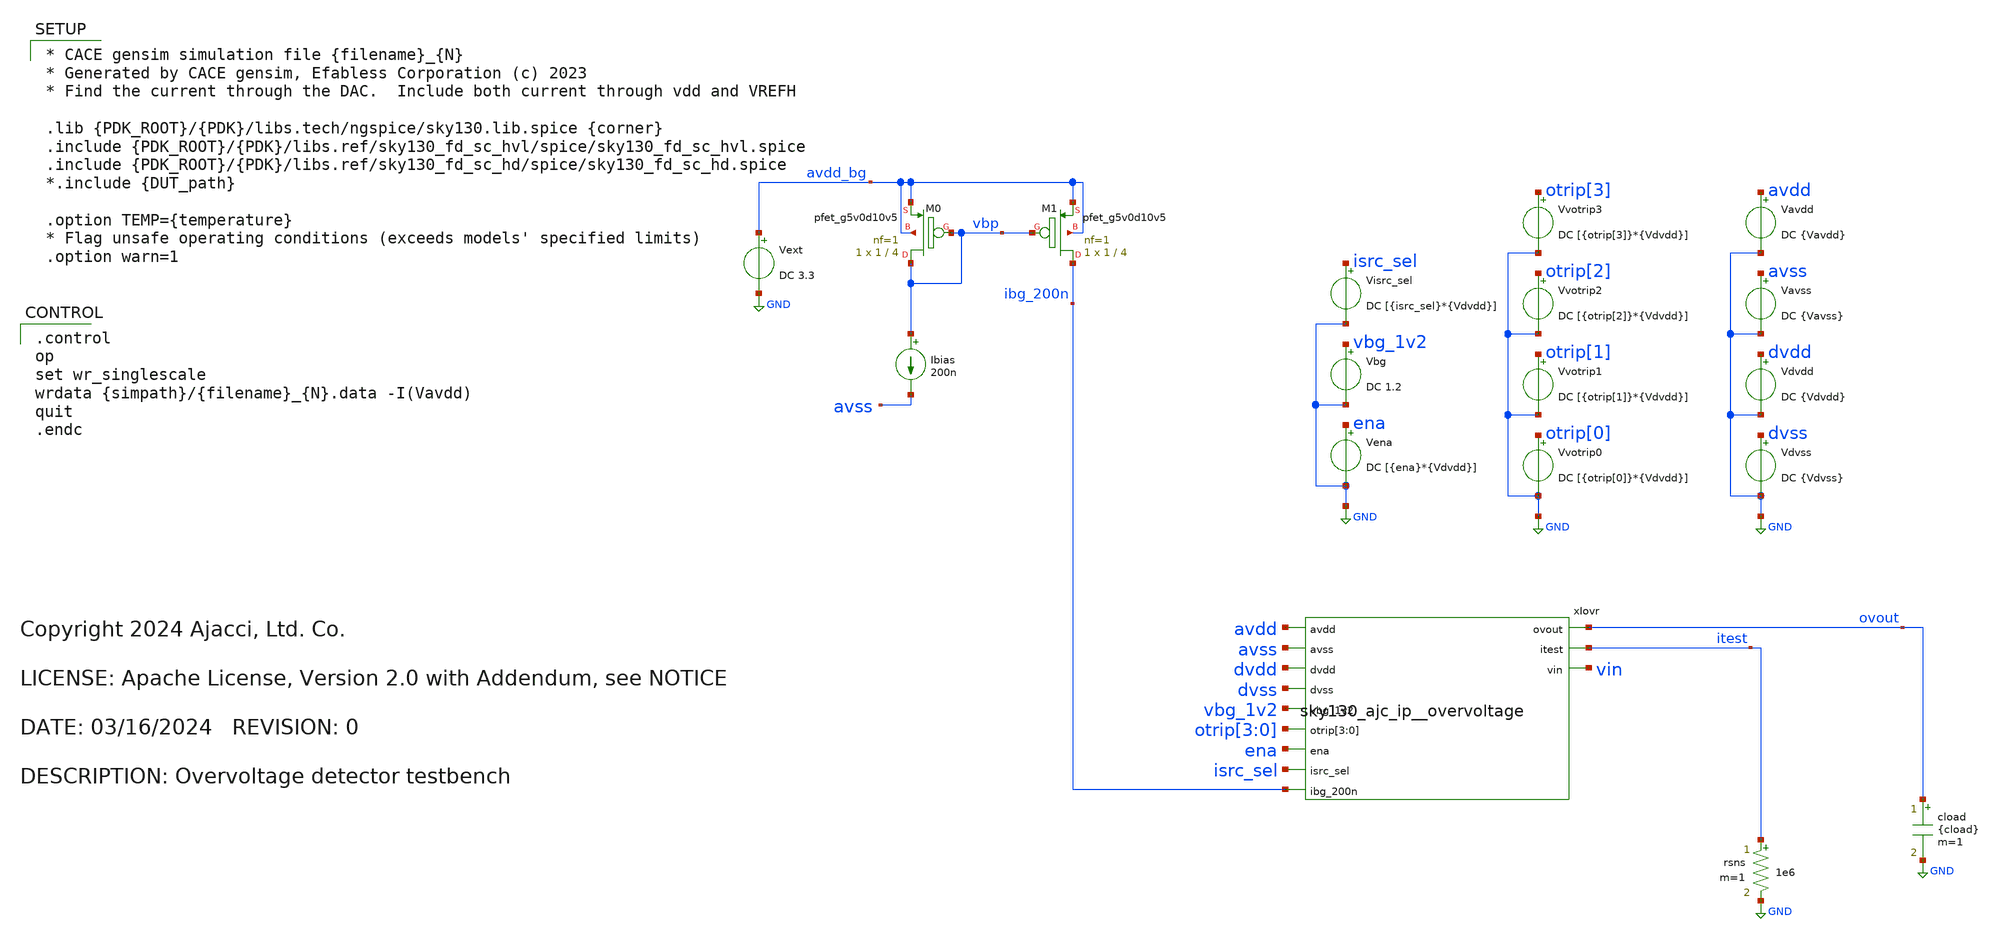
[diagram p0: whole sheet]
** sch_path: cace/dccurrent_avdd.sch
* Copyright 2024 Ajacci, Ltd. Co.
* LICENSE: Apache License, Version 2.0 with Addendum, see NOTICE
**.subckt dccurrent_avdd
Vavss avss GND DC {Vavss}
Vena ena GND DC [{ena}*{Vdvdd}]
Vavdd avdd GND DC {Vavdd}
.save i(vavdd)
Vbg vbg_1v2 GND DC 1.2
Ibias vbp avss 200n
XM1 ibg_200n vbp avdd_bg avdd_bg sky130_fd_pr__pfet_g5v0d10v5 L=4 W=1 nf=1 ad='int((nf+1)/2) * W/nf * 0.29'
+ as='int((nf+2)/2) * W/nf * 0.29' pd='2*int((nf+1)/2) * (W/nf + 0.29)' ps='2*int((nf+2)/2) * (W/nf + 0.29)'
+ nrd='0.29 / W' nrs='0.29 / W' sa=0 sb=0 sd=0 mult=1 m=1
XM0 vbp vbp avdd_bg avdd_bg sky130_fd_pr__pfet_g5v0d10v5 L=4 W=1 nf=1 ad='int((nf+1)/2) * W/nf * 0.29'
+ as='int((nf+2)/2) * W/nf * 0.29' pd='2*int((nf+1)/2) * (W/nf + 0.29)' ps='2*int((nf+2)/2) * (W/nf + 0.29)'
+ nrd='0.29 / W' nrs='0.29 / W' sa=0 sb=0 sd=0 mult=1 m=1
Vdvss dvss GND DC {Vdvss}
Vdvdd dvdd GND DC {Vdvdd}
.save i(vdvdd)
rsns itest GND 1e6 m=1
cload ovout GND {cload} m=1
xIovr avdd avss dvdd dvss vbg_1v2 ovout itest otrip[3] otrip[2] otrip[1] otrip[0] vin ena isrc_sel
+ ibg_200n sky130_ajc_ip__overvoltage
Vvotrip0 otrip[0] GND DC [{otrip[0]}*{Vdvdd}]
.save i(vvotrip0)
Vvotrip1 otrip[1] GND DC [{otrip[1]}*{Vdvdd}]
.save i(vvotrip1)
Vvotrip2 otrip[2] GND DC [{otrip[2]}*{Vdvdd}]
.save i(vvotrip2)
Vvotrip3 otrip[3] GND DC [{otrip[3]}*{Vdvdd}]
.save i(vvotrip3)
Visrc_sel isrc_sel GND DC [{isrc_sel}*{Vdvdd}]
Vext avdd_bg GND DC 3.3
.save i(vext)
**** begin user architecture code

* CACE gensim simulation file {filename}_{N}
* Generated by CACE gensim, Efabless Corporation (c) 2023
* Find the current through the DAC.  Include both current through vdd and VREFH

.lib {PDK_ROOT}/{PDK}/libs.tech/ngspice/sky130.lib.spice {corner}
.include {PDK_ROOT}/{PDK}/libs.ref/sky130_fd_sc_hvl/spice/sky130_fd_sc_hvl.spice
.include {PDK_ROOT}/{PDK}/libs.ref/sky130_fd_sc_hd/spice/sky130_fd_sc_hd.spice
*.include {DUT_path}

.option TEMP={temperature}
* Flag unsafe operating conditions (exceeds models' specified limits)
.option warn=1



.control
op
set wr_singlescale
wrdata {simpath}/{filename}_{N}.data -I(Vavdd)
quit
.endc


**** end user architecture code
**.ends
.GLOBAL GND
.end
